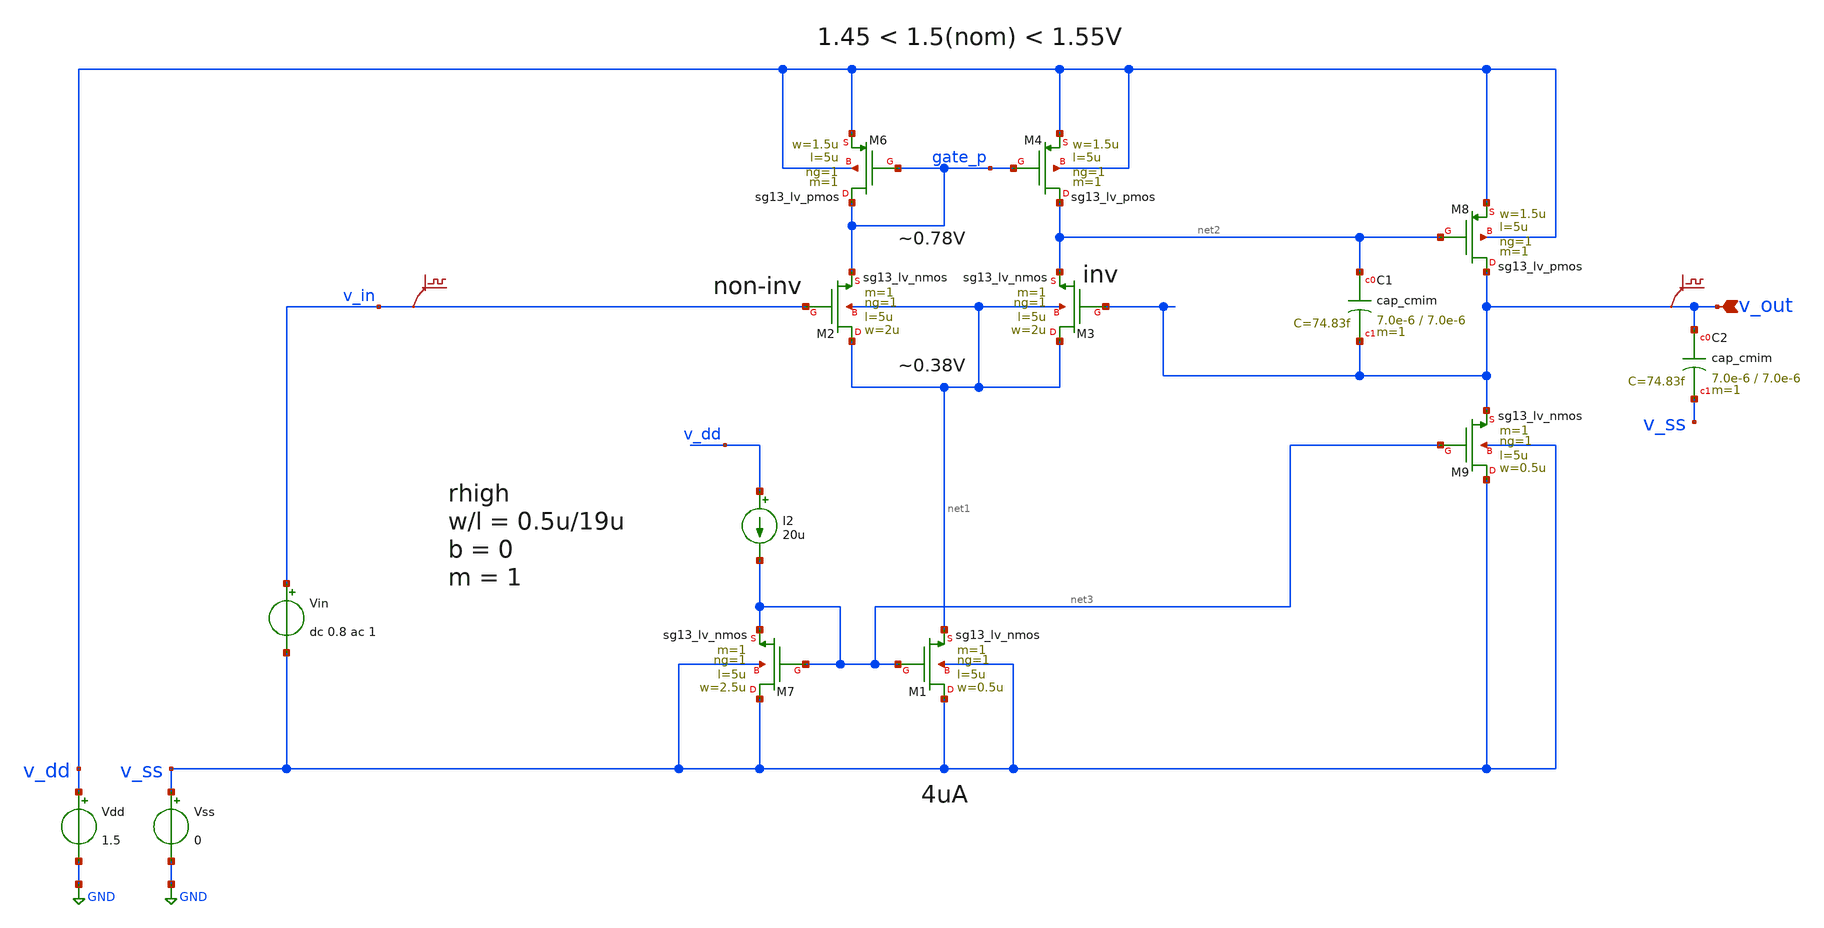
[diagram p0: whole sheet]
** sch_path: 3_Real_Cir/10_Real_Cir/test_Real_Cir/Improved/improved_5t_ota_tb_A.sch
* Copyright 2023 IHP PDK Authors
* Licensed under the Apache License, Version 2.0 (the "License");
* you may not use this file except in compliance with the License.
* You may obtain a copy of the License at
* https://www.apache.org/licenses/LICENSE-2.0
* Unless required by applicable law or agreed to in writing, software
* distributed under the License is distributed on an "AS IS" BASIS,
* WITHOUT WARRANTIES OR CONDITIONS OF ANY KIND, either express or implied.
* See the License for the specific language governing permissions and
* limitations under the License.
* Copyright 2024 IHP PDK Authors
**.subckt improved_5t_ota_tb_A v_out
*.ipin v_out
Vdd v_dd GND 1.5
Vss v_ss GND 0
Vin v_in v_ss dc 0.8 ac 1
.save v(v_in)
.save v(v_out)
XM1 v_ss net3 net1 v_ss sg13_lv_nmos w=0.5u l=5u ng=1 m=1 mm_ok=1
XM4 net2 gate_p v_dd v_dd sg13_lv_pmos w=1.5u l=5u ng=1 m=1 mm_ok=1
XM2 net1 v_in gate_p net1 sg13_lv_nmos w=2u l=5u ng=1 m=1 mm_ok=1
XM3 net1 v_out net2 net1 sg13_lv_nmos w=2u l=5u ng=1 m=1 mm_ok=1
XM6 gate_p gate_p v_dd v_dd sg13_lv_pmos w=1.5u l=5u ng=1 m=1 mm_ok=1
XM7 v_ss net3 net3 v_ss sg13_lv_nmos w=2.5u l=5u ng=1 m=1 mm_ok=1
XM8 v_out net2 v_dd v_dd sg13_lv_pmos w=1.5u l=5u ng=1 m=1 mm_ok=1
XM9 v_ss net3 v_out v_ss sg13_lv_nmos w=0.5u l=5u ng=1 m=1 mm_ok=1
XC1 net2 v_out cap_cmim w=7.0e-6 l=7.0e-6 m=1 mm_ok=1
I2 v_dd net3 20u
XC2 v_out v_ss cap_cmim w=7.0e-6 l=7.0e-6 m=1 mm_ok=1
**** begin user architecture code


.temp 27
.control
option sparse
save all
op
write ota-5t_tb-ac.raw
set appendwrite

ac dec 101 1k 100MEG
write ota-5t_tb-ac.raw

.title Mein Schwein pfeift

plot 20*log10(v_out) xlabel notimeforcaution ylabel atten(ua)tion/gain

meas ac dcgain MAX vmag(v_out) FROM=10 TO=10k
let f3db = dcgain/sqrt(2)
meas ac fbw WHEN vmag(v_out)=f3db FALL=1
let gainerror=(dcgain-1)/1
print dcgain
print fbw
print gainerror

noise v(v_out) Vin dec 101 1k 100MEG
print onoise_total

.endc


 .lib cornerMOSlv.lib mos_tt

 .lib $::SG13G2_MODELS/cornerMOSlv.lib mos_tt
.lib $::SG13G2_MODELS/cornerCAP.lib cap_typ
.inc $::PDK_ROOT/ihp-sg13g2/libs.ref/sg13g2_stdcell/spice/sg13g2_stdcell.spice

**** end user architecture code
**.ends
.GLOBAL GND
.end
